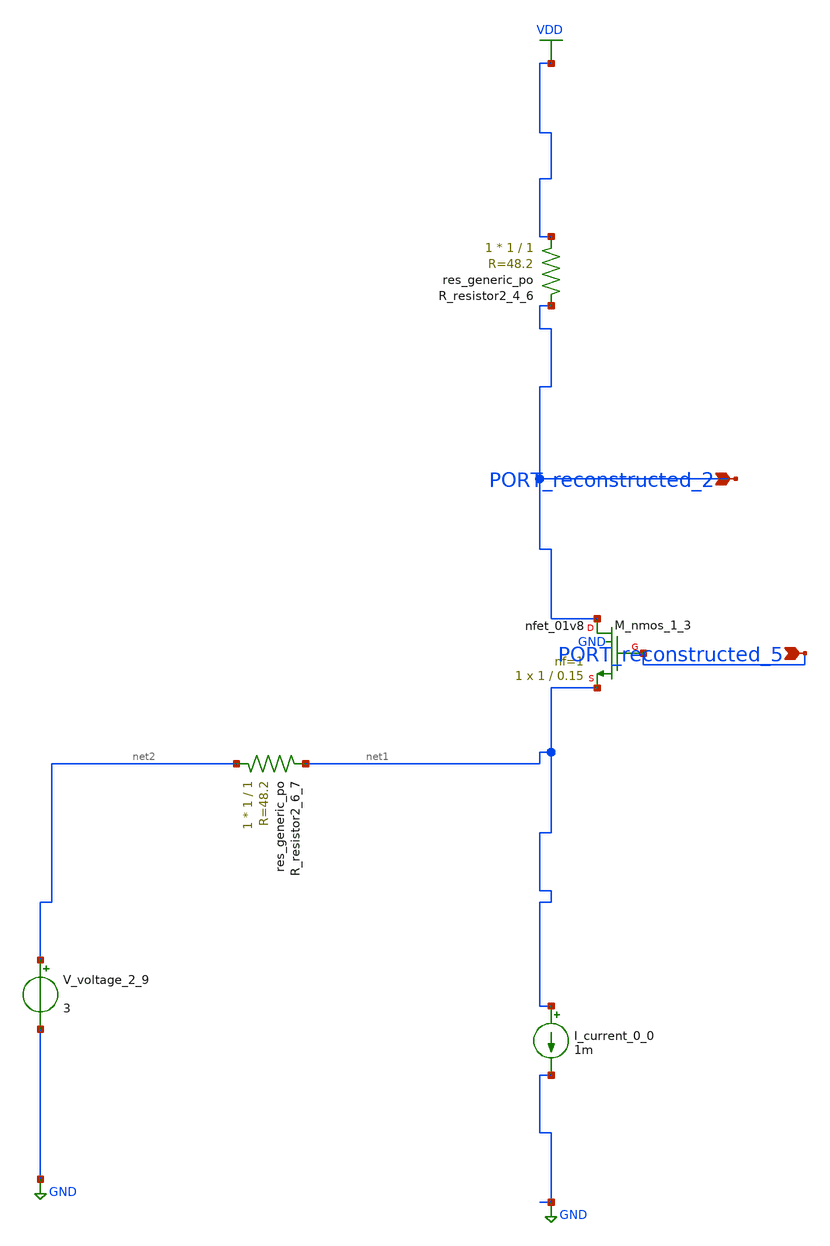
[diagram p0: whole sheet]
** sch_path: schematics/AMSNet/360.sch
**.subckt 360 PORT_reconstructed_5 PORT_reconstructed_2
*.ipin PORT_reconstructed_5
*.ipin PORT_reconstructed_2
I_current_0_0 net1 GND 1m
XM_nmos_1_3 PORT_reconstructed_2 PORT_reconstructed_5 net1 GND sky130_fd_pr__nfet_01v8 L=0.15 W=1 nf=1
+ ad='int((1 + 1)/2) * 1 / 1 * 0.29' as='int((1 + 2)/2) * 1 / 1 * 0.29' pd='2*int((1 + 1)/2) * (1 / 1 + 0.29)'
+ ps='2*int((1 + 2)/2) * (1 / 1 + 0.29)' nrd='0.29 / 1 ' nrs='0.29 / 1 ' sa=0 sb=0 sd=0 mult=1 m=1
XR_resistor2_4_6 VDD PORT_reconstructed_2 sky130_fd_pr__res_generic_po W=1 L=1 m=1
XR_resistor2_6_7 net2 net1 sky130_fd_pr__res_generic_po W=1 L=1 m=1
V_voltage_2_9 net2 GND 3
**.ends
.GLOBAL GND
.GLOBAL VDD
.end
